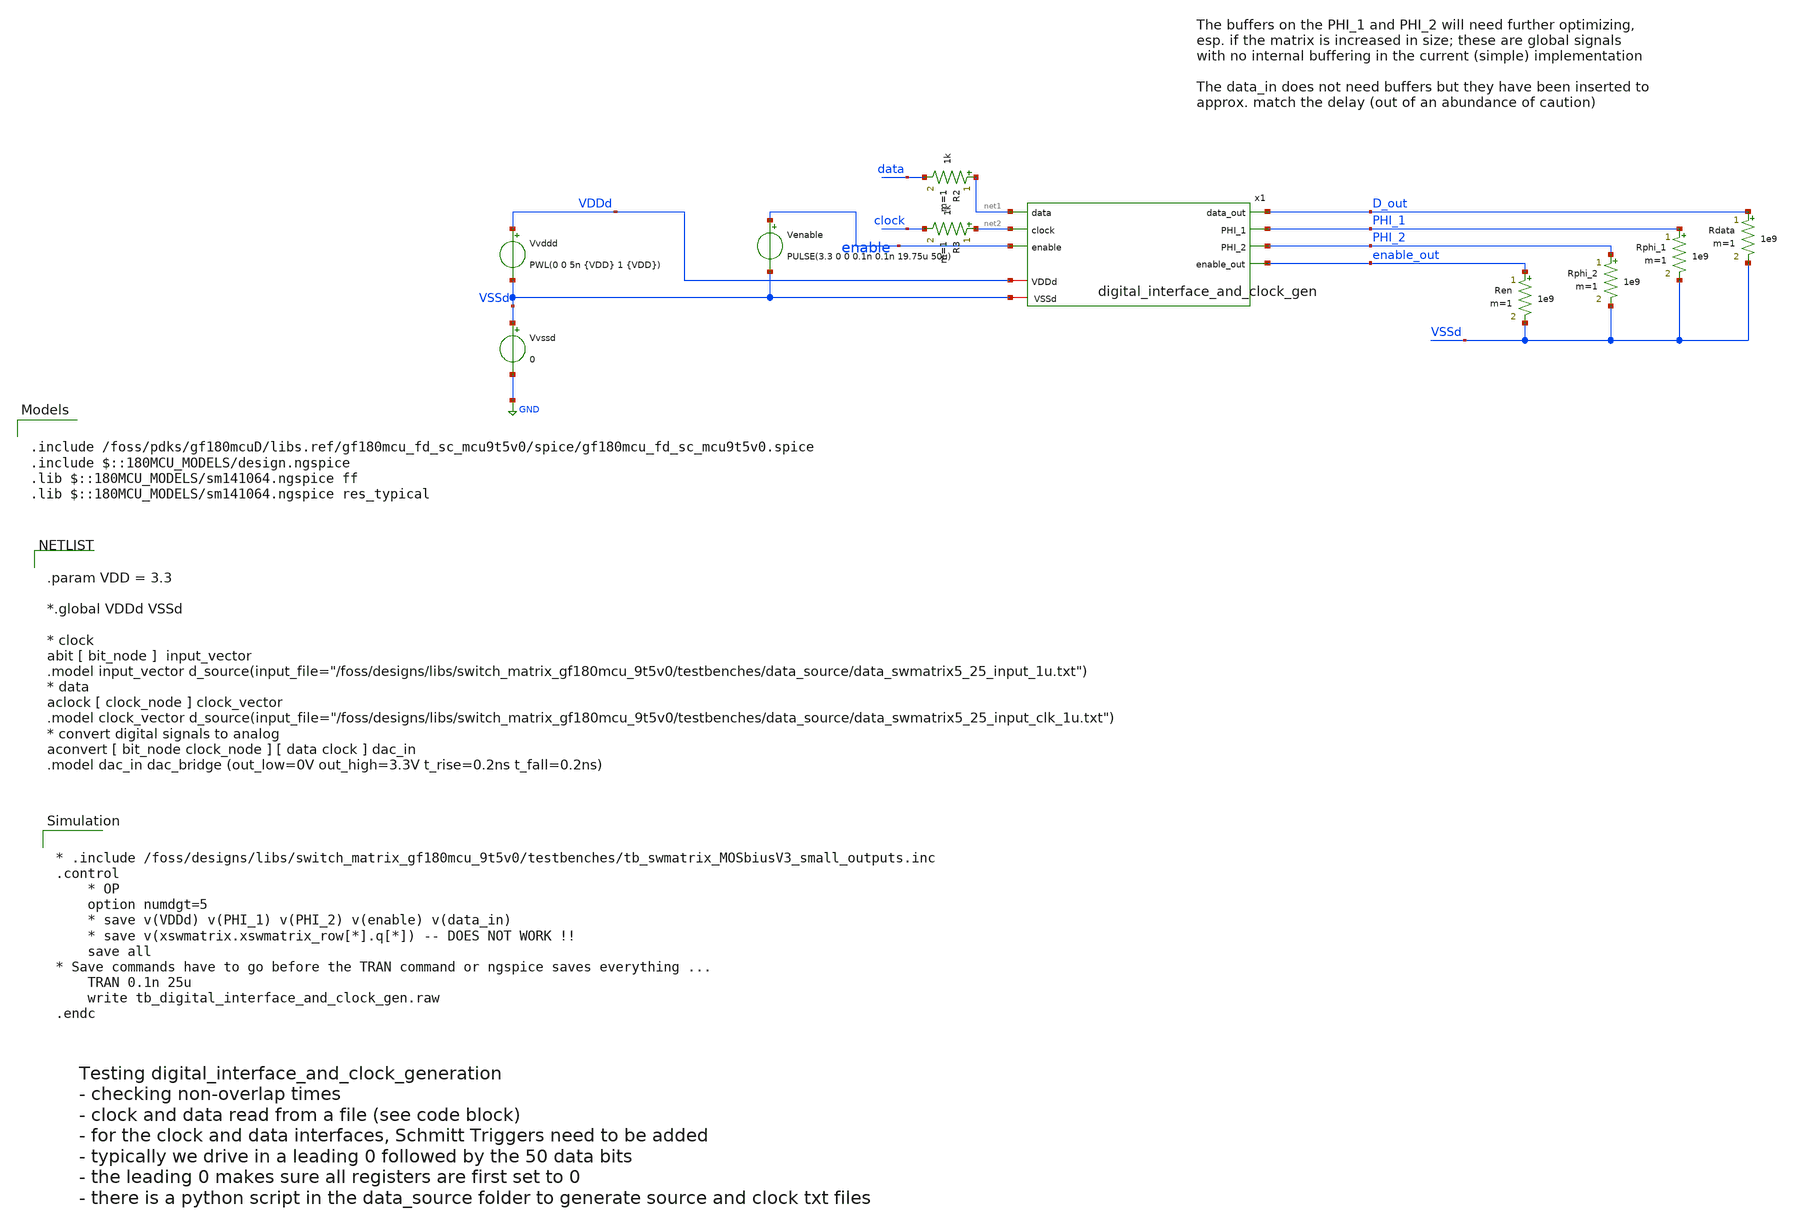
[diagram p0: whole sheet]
** sch_path: testbenches/tb_digital_interface_and_clock_gen.sch
**.subckt tb_digital_interface_and_clock_gen
Vvssd VSSd GND 0
Vvddd VDDd VSSd PWL(0 0 5n {VDD} 1 {VDD})
Venable enable VSSd PULSE(3.3 0 0 0.1n 0.1n 19.75u 50u)
R2 net1 data 1k m=1
R3 net2 clock 1k m=1
Ren enable_out VSSd 1e9 m=1
Rphi_2 PHI_2 VSSd 1e9 m=1
Rphi_1 PHI_1 VSSd 1e9 m=1
Rdata D_out VSSd 1e9 m=1
x1 net1 D_out net2 PHI_1 PHI_2 enable enable_out VDDd VSSd digital_interface_and_clock_gen
**** begin user architecture code


* .include
*+ /foss/designs/libs/switch_matrix_gf180mcu_9t5v0/testbenches/tb_swmatrix_MOSbiusV3_small_outputs.inc
.control
    * OP
    option numdgt=5
    * save v(VDDd) v(PHI_1) v(PHI_2) v(enable) v(data_in)
    * save v(xswmatrix.xswmatrix_row[*].q[*]) -- DOES NOT WORK !!
    save all
* Save commands have to go before the TRAN command or ngspice saves everything ...
    TRAN 0.1n 25u
    write tb_digital_interface_and_clock_gen.raw
.endc



.include /foss/pdks/gf180mcuD/libs.ref/gf180mcu_fd_sc_mcu9t5v0/spice/gf180mcu_fd_sc_mcu9t5v0.spice
.include $::180MCU_MODELS/design.ngspice
.lib $::180MCU_MODELS/sm141064.ngspice ff
.lib $::180MCU_MODELS/sm141064.ngspice res_typical



.param VDD = 3.3

*.global VDDd VSSd

* clock
abit [ bit_node ]  input_vector
.model input_vector
+ d_source(input_file="/foss/designs/libs/switch_matrix_gf180mcu_9t5v0/testbenches/data_source/data_swmatrix5_25_input_1u.txt")
* data
aclock [ clock_node ] clock_vector
.model clock_vector
+ d_source(input_file="/foss/designs/libs/switch_matrix_gf180mcu_9t5v0/testbenches/data_source/data_swmatrix5_25_input_clk_1u.txt")
* convert digital signals to analog
aconvert [ bit_node clock_node ] [ data clock ] dac_in
.model dac_in dac_bridge (out_low=0V out_high=3.3V t_rise=0.2ns t_fall=0.2ns)


**** end user architecture code
**.ends

* expanding   symbol:
*+  switch_matrix_gf180mcu_9t5v0/digital_interface_and_clock_gen/digital_interface_and_clock_gen.sym # of pins=9
** sym_path: digital_interface_and_clock_gen/digital_interface_and_clock_gen.sym
** sch_path: digital_interface_and_clock_gen/digital_interface_and_clock_gen.sch
.subckt digital_interface_and_clock_gen data data_out clock PHI_1 PHI_2 enable enable_out VDDd VSSd
*.ipin data
*.ipin clock
*.ipin enable
*.iopin VSSd
*.iopin VDDd
*.opin data_out
*.opin PHI_1
*.opin PHI_2
*.opin enable_out
xNO_ClkGen PHI_2_gen clock_gated PHI_1_gen VDDd VSSd NO_ClkGen
x6 PHI_2_gen VSSd VDDd VSSd VDDd net1 gf180mcu_fd_sc_mcu9t5v0__inv_4
x7 net1 VSSd VDDd VSSd VDDd PHI_2 gf180mcu_fd_sc_mcu9t5v0__inv_8
x9 PHI_1_gen VSSd VDDd VSSd VDDd net2 gf180mcu_fd_sc_mcu9t5v0__inv_4
x10 net2 VSSd VDDd VSSd VDDd PHI_1 gf180mcu_fd_sc_mcu9t5v0__inv_8
x12 data_gated VSSd VDDd VSSd VDDd net3 gf180mcu_fd_sc_mcu9t5v0__inv_4
x13 net3 VSSd VDDd VSSd VDDd net8 gf180mcu_fd_sc_mcu9t5v0__inv_8
x2 net7 VSSd VDDd VSSd VDDd net4 gf180mcu_fd_sc_mcu9t5v0__inv_4
x8 net4 VSSd VDDd VSSd VDDd enable_out gf180mcu_fd_sc_mcu9t5v0__inv_8
x11 net5 net4 VSSd VDDd VSSd VDDd net10 gf180mcu_fd_sc_mcu9t5v0__nand2_4
x4 net6 net4 VSSd VDDd VSSd VDDd net11 gf180mcu_fd_sc_mcu9t5v0__nand2_4
x1 net11 VSSd VDDd VSSd VDDd clock_gated gf180mcu_fd_sc_mcu9t5v0__inv_4
x3 net10 VSSd VDDd VSSd VDDd data_gated gf180mcu_fd_sc_mcu9t5v0__inv_4
x5 VDDd clock net6 VSSd Schmitt
x14 VDDd data net5 VSSd Schmitt
x15 VDDd enable net7 VSSd Schmitt
XR1 VSSd enable VSSd ppolyf_u_1k r_width=1e-6 r_length=20e-6 m=2
x16 net8 VSSd VDDd VSSd VDDd net9 gf180mcu_fd_sc_mcu9t5v0__inv_12
x17 net9 data_out VDDd VDDd VSSd VSSd gf180mcu_fd_sc_mcu9t5v0__inv_20
.ends


* expanding   symbol:  switch_matrix_gf180mcu_9t5v0/NO_ClkGen/NO_ClkGen.sym # of pins=5
** sym_path: switch_matrix_gf180mcu_9t5v0/NO_ClkGen/NO_ClkGen.sym
** sch_path: switch_matrix_gf180mcu_9t5v0/NO_ClkGen/NO_ClkGen.sch
.subckt NO_ClkGen PHI_2 CLK PHI_1 VDDd VSSd
*.ipin CLK
*.opin PHI_2
*.opin PHI_1
*.iopin VDDd
*.iopin VSSd
x1 CLKB OUT_bot_d VSSd VDDd VSSd VDDd OUT_top gf180mcu_fd_sc_mcu9t5v0__nand2_1
x2 OUT_top_d CLKbuf VSSd VDDd VSSd VDDd OUT_bot gf180mcu_fd_sc_mcu9t5v0__nand2_1
x3 OUT_top VSSd VDDd VSSd VDDd PHI_2 gf180mcu_fd_sc_mcu9t5v0__inv_1
x4 PHI_2 VSSd VDDd VSSd VDDd in_d_2 gf180mcu_fd_sc_mcu9t5v0__inv_1
x6 OUT_bot VSSd VDDd VSSd VDDd PHI_1 gf180mcu_fd_sc_mcu9t5v0__inv_1
x9 CLKB VSSd VDDd VSSd VDDd CLKbuf gf180mcu_fd_sc_mcu9t5v0__inv_1
x10 CLK VSSd VDDd VSSd VDDd CLKB gf180mcu_fd_sc_mcu9t5v0__inv_1
* noconn VDDd
* noconn VSSd
xinv1[1] in_d_2 VSSd VDDd VSSd VDDd out_2[1] gf180mcu_fd_sc_mcu9t5v0__inv_1
xinv1[2] out_2[1] VSSd VDDd VSSd VDDd out_2[2] gf180mcu_fd_sc_mcu9t5v0__inv_1
xinv1[3] out_2[2] VSSd VDDd VSSd VDDd out_2[3] gf180mcu_fd_sc_mcu9t5v0__inv_1
xinv1[4] out_2[3] VSSd VDDd VSSd VDDd out_2[4] gf180mcu_fd_sc_mcu9t5v0__inv_1
xinv1[5] out_2[4] VSSd VDDd VSSd VDDd out_2[5] gf180mcu_fd_sc_mcu9t5v0__inv_1
xinv1[6] out_2[5] VSSd VDDd VSSd VDDd out_2[6] gf180mcu_fd_sc_mcu9t5v0__inv_1
xinv1[7] out_2[6] VSSd VDDd VSSd VDDd out_2[7] gf180mcu_fd_sc_mcu9t5v0__inv_1
xinv1[8] out_2[7] VSSd VDDd VSSd VDDd out_2[8] gf180mcu_fd_sc_mcu9t5v0__inv_1
xinv1[9] out_2[8] VSSd VDDd VSSd VDDd out_2[9] gf180mcu_fd_sc_mcu9t5v0__inv_1
xinv1[10] out_2[9] VSSd VDDd VSSd VDDd out_2[10] gf180mcu_fd_sc_mcu9t5v0__inv_1
xinv1[11] out_2[10] VSSd VDDd VSSd VDDd out_2[11] gf180mcu_fd_sc_mcu9t5v0__inv_1
xinv1[12] out_2[11] VSSd VDDd VSSd VDDd out_2[12] gf180mcu_fd_sc_mcu9t5v0__inv_1
xinv1[13] out_2[12] VSSd VDDd VSSd VDDd out_2[13] gf180mcu_fd_sc_mcu9t5v0__inv_1
xinv1[14] out_2[13] VSSd VDDd VSSd VDDd out_2[14] gf180mcu_fd_sc_mcu9t5v0__inv_1
xinv1[15] out_2[14] VSSd VDDd VSSd VDDd out_2[15] gf180mcu_fd_sc_mcu9t5v0__inv_1
xinv1[16] out_2[15] VSSd VDDd VSSd VDDd out_2[16] gf180mcu_fd_sc_mcu9t5v0__inv_1
xinv1[17] out_2[16] VSSd VDDd VSSd VDDd out_2[17] gf180mcu_fd_sc_mcu9t5v0__inv_1
xinv1[18] out_2[17] VSSd VDDd VSSd VDDd out_2[18] gf180mcu_fd_sc_mcu9t5v0__inv_1
xinv1[19] out_2[18] VSSd VDDd VSSd VDDd out_2[19] gf180mcu_fd_sc_mcu9t5v0__inv_1
xinv1[20] out_2[19] VSSd VDDd VSSd VDDd OUT_top_d gf180mcu_fd_sc_mcu9t5v0__inv_1
x5 PHI_1 VSSd VDDd VSSd VDDd in_d_1 gf180mcu_fd_sc_mcu9t5v0__inv_1
xinv2[1] in_d_1 VSSd VDDd VSSd VDDd out_1[1] gf180mcu_fd_sc_mcu9t5v0__inv_1
xinv2[2] out_1[1] VSSd VDDd VSSd VDDd out_1[2] gf180mcu_fd_sc_mcu9t5v0__inv_1
xinv2[3] out_1[2] VSSd VDDd VSSd VDDd out_1[3] gf180mcu_fd_sc_mcu9t5v0__inv_1
xinv2[4] out_1[3] VSSd VDDd VSSd VDDd out_1[4] gf180mcu_fd_sc_mcu9t5v0__inv_1
xinv2[5] out_1[4] VSSd VDDd VSSd VDDd out_1[5] gf180mcu_fd_sc_mcu9t5v0__inv_1
xinv2[6] out_1[5] VSSd VDDd VSSd VDDd out_1[6] gf180mcu_fd_sc_mcu9t5v0__inv_1
xinv2[7] out_1[6] VSSd VDDd VSSd VDDd out_1[7] gf180mcu_fd_sc_mcu9t5v0__inv_1
xinv2[8] out_1[7] VSSd VDDd VSSd VDDd out_1[8] gf180mcu_fd_sc_mcu9t5v0__inv_1
xinv2[9] out_1[8] VSSd VDDd VSSd VDDd out_1[9] gf180mcu_fd_sc_mcu9t5v0__inv_1
xinv2[10] out_1[9] VSSd VDDd VSSd VDDd out_1[10] gf180mcu_fd_sc_mcu9t5v0__inv_1
xinv2[11] out_1[10] VSSd VDDd VSSd VDDd out_1[11] gf180mcu_fd_sc_mcu9t5v0__inv_1
xinv2[12] out_1[11] VSSd VDDd VSSd VDDd out_1[12] gf180mcu_fd_sc_mcu9t5v0__inv_1
xinv2[13] out_1[12] VSSd VDDd VSSd VDDd out_1[13] gf180mcu_fd_sc_mcu9t5v0__inv_1
xinv2[14] out_1[13] VSSd VDDd VSSd VDDd out_1[14] gf180mcu_fd_sc_mcu9t5v0__inv_1
xinv2[15] out_1[14] VSSd VDDd VSSd VDDd out_1[15] gf180mcu_fd_sc_mcu9t5v0__inv_1
xinv2[16] out_1[15] VSSd VDDd VSSd VDDd out_1[16] gf180mcu_fd_sc_mcu9t5v0__inv_1
xinv2[17] out_1[16] VSSd VDDd VSSd VDDd out_1[17] gf180mcu_fd_sc_mcu9t5v0__inv_1
xinv2[18] out_1[17] VSSd VDDd VSSd VDDd out_1[18] gf180mcu_fd_sc_mcu9t5v0__inv_1
xinv2[19] out_1[18] VSSd VDDd VSSd VDDd out_1[19] gf180mcu_fd_sc_mcu9t5v0__inv_1
xinv2[20] out_1[19] VSSd VDDd VSSd VDDd OUT_bot_d gf180mcu_fd_sc_mcu9t5v0__inv_1
XMcapbot[1] VSSd out_1[1] VSSd VSSd nfet_03v3 L=1u W=25u nf=5 ad='int((nf+1)/2) * W/nf * 0.18u' as='int((nf+2)/2) * W/nf * 0.18u'
+ pd='2*int((nf+1)/2) * (W/nf + 0.18u)' ps='2*int((nf+2)/2) * (W/nf + 0.18u)' nrd='0.18u / W' nrs='0.18u / W'
+ sa=0 sb=0 sd=0 m=1
XMcapbot[2] VSSd out_1[2] VSSd VSSd nfet_03v3 L=1u W=25u nf=5 ad='int((nf+1)/2) * W/nf * 0.18u' as='int((nf+2)/2) * W/nf * 0.18u'
+ pd='2*int((nf+1)/2) * (W/nf + 0.18u)' ps='2*int((nf+2)/2) * (W/nf + 0.18u)' nrd='0.18u / W' nrs='0.18u / W'
+ sa=0 sb=0 sd=0 m=1
XMcapbot[3] VSSd out_1[3] VSSd VSSd nfet_03v3 L=1u W=25u nf=5 ad='int((nf+1)/2) * W/nf * 0.18u' as='int((nf+2)/2) * W/nf * 0.18u'
+ pd='2*int((nf+1)/2) * (W/nf + 0.18u)' ps='2*int((nf+2)/2) * (W/nf + 0.18u)' nrd='0.18u / W' nrs='0.18u / W'
+ sa=0 sb=0 sd=0 m=1
XMcapbot[4] VSSd out_1[4] VSSd VSSd nfet_03v3 L=1u W=25u nf=5 ad='int((nf+1)/2) * W/nf * 0.18u' as='int((nf+2)/2) * W/nf * 0.18u'
+ pd='2*int((nf+1)/2) * (W/nf + 0.18u)' ps='2*int((nf+2)/2) * (W/nf + 0.18u)' nrd='0.18u / W' nrs='0.18u / W'
+ sa=0 sb=0 sd=0 m=1
XMcapbot[5] VSSd out_1[5] VSSd VSSd nfet_03v3 L=1u W=25u nf=5 ad='int((nf+1)/2) * W/nf * 0.18u' as='int((nf+2)/2) * W/nf * 0.18u'
+ pd='2*int((nf+1)/2) * (W/nf + 0.18u)' ps='2*int((nf+2)/2) * (W/nf + 0.18u)' nrd='0.18u / W' nrs='0.18u / W'
+ sa=0 sb=0 sd=0 m=1
XMcapbot[6] VSSd out_1[6] VSSd VSSd nfet_03v3 L=1u W=25u nf=5 ad='int((nf+1)/2) * W/nf * 0.18u' as='int((nf+2)/2) * W/nf * 0.18u'
+ pd='2*int((nf+1)/2) * (W/nf + 0.18u)' ps='2*int((nf+2)/2) * (W/nf + 0.18u)' nrd='0.18u / W' nrs='0.18u / W'
+ sa=0 sb=0 sd=0 m=1
XMcapbot[7] VSSd out_1[7] VSSd VSSd nfet_03v3 L=1u W=25u nf=5 ad='int((nf+1)/2) * W/nf * 0.18u' as='int((nf+2)/2) * W/nf * 0.18u'
+ pd='2*int((nf+1)/2) * (W/nf + 0.18u)' ps='2*int((nf+2)/2) * (W/nf + 0.18u)' nrd='0.18u / W' nrs='0.18u / W'
+ sa=0 sb=0 sd=0 m=1
XMcapbot[8] VSSd out_1[8] VSSd VSSd nfet_03v3 L=1u W=25u nf=5 ad='int((nf+1)/2) * W/nf * 0.18u' as='int((nf+2)/2) * W/nf * 0.18u'
+ pd='2*int((nf+1)/2) * (W/nf + 0.18u)' ps='2*int((nf+2)/2) * (W/nf + 0.18u)' nrd='0.18u / W' nrs='0.18u / W'
+ sa=0 sb=0 sd=0 m=1
XMcapbot[9] VSSd out_1[9] VSSd VSSd nfet_03v3 L=1u W=25u nf=5 ad='int((nf+1)/2) * W/nf * 0.18u' as='int((nf+2)/2) * W/nf * 0.18u'
+ pd='2*int((nf+1)/2) * (W/nf + 0.18u)' ps='2*int((nf+2)/2) * (W/nf + 0.18u)' nrd='0.18u / W' nrs='0.18u / W'
+ sa=0 sb=0 sd=0 m=1
XMcapbot[10] VSSd out_1[10] VSSd VSSd nfet_03v3 L=1u W=25u nf=5 ad='int((nf+1)/2) * W/nf * 0.18u' as='int((nf+2)/2) * W/nf * 0.18u'
+ pd='2*int((nf+1)/2) * (W/nf + 0.18u)' ps='2*int((nf+2)/2) * (W/nf + 0.18u)' nrd='0.18u / W' nrs='0.18u / W'
+ sa=0 sb=0 sd=0 m=1
XMcapbot[11] VSSd out_1[11] VSSd VSSd nfet_03v3 L=1u W=25u nf=5 ad='int((nf+1)/2) * W/nf * 0.18u' as='int((nf+2)/2) * W/nf * 0.18u'
+ pd='2*int((nf+1)/2) * (W/nf + 0.18u)' ps='2*int((nf+2)/2) * (W/nf + 0.18u)' nrd='0.18u / W' nrs='0.18u / W'
+ sa=0 sb=0 sd=0 m=1
XMcapbot[12] VSSd out_1[12] VSSd VSSd nfet_03v3 L=1u W=25u nf=5 ad='int((nf+1)/2) * W/nf * 0.18u' as='int((nf+2)/2) * W/nf * 0.18u'
+ pd='2*int((nf+1)/2) * (W/nf + 0.18u)' ps='2*int((nf+2)/2) * (W/nf + 0.18u)' nrd='0.18u / W' nrs='0.18u / W'
+ sa=0 sb=0 sd=0 m=1
XMcapbot[13] VSSd out_1[13] VSSd VSSd nfet_03v3 L=1u W=25u nf=5 ad='int((nf+1)/2) * W/nf * 0.18u' as='int((nf+2)/2) * W/nf * 0.18u'
+ pd='2*int((nf+1)/2) * (W/nf + 0.18u)' ps='2*int((nf+2)/2) * (W/nf + 0.18u)' nrd='0.18u / W' nrs='0.18u / W'
+ sa=0 sb=0 sd=0 m=1
XMcapbot[14] VSSd out_1[14] VSSd VSSd nfet_03v3 L=1u W=25u nf=5 ad='int((nf+1)/2) * W/nf * 0.18u' as='int((nf+2)/2) * W/nf * 0.18u'
+ pd='2*int((nf+1)/2) * (W/nf + 0.18u)' ps='2*int((nf+2)/2) * (W/nf + 0.18u)' nrd='0.18u / W' nrs='0.18u / W'
+ sa=0 sb=0 sd=0 m=1
XMcapbot[15] VSSd out_1[15] VSSd VSSd nfet_03v3 L=1u W=25u nf=5 ad='int((nf+1)/2) * W/nf * 0.18u' as='int((nf+2)/2) * W/nf * 0.18u'
+ pd='2*int((nf+1)/2) * (W/nf + 0.18u)' ps='2*int((nf+2)/2) * (W/nf + 0.18u)' nrd='0.18u / W' nrs='0.18u / W'
+ sa=0 sb=0 sd=0 m=1
XMcapbot[16] VSSd out_1[16] VSSd VSSd nfet_03v3 L=1u W=25u nf=5 ad='int((nf+1)/2) * W/nf * 0.18u' as='int((nf+2)/2) * W/nf * 0.18u'
+ pd='2*int((nf+1)/2) * (W/nf + 0.18u)' ps='2*int((nf+2)/2) * (W/nf + 0.18u)' nrd='0.18u / W' nrs='0.18u / W'
+ sa=0 sb=0 sd=0 m=1
XMcapbot[17] VSSd out_1[17] VSSd VSSd nfet_03v3 L=1u W=25u nf=5 ad='int((nf+1)/2) * W/nf * 0.18u' as='int((nf+2)/2) * W/nf * 0.18u'
+ pd='2*int((nf+1)/2) * (W/nf + 0.18u)' ps='2*int((nf+2)/2) * (W/nf + 0.18u)' nrd='0.18u / W' nrs='0.18u / W'
+ sa=0 sb=0 sd=0 m=1
XMcapbot[18] VSSd out_1[18] VSSd VSSd nfet_03v3 L=1u W=25u nf=5 ad='int((nf+1)/2) * W/nf * 0.18u' as='int((nf+2)/2) * W/nf * 0.18u'
+ pd='2*int((nf+1)/2) * (W/nf + 0.18u)' ps='2*int((nf+2)/2) * (W/nf + 0.18u)' nrd='0.18u / W' nrs='0.18u / W'
+ sa=0 sb=0 sd=0 m=1
XMcapbot[19] VSSd out_1[19] VSSd VSSd nfet_03v3 L=1u W=25u nf=5 ad='int((nf+1)/2) * W/nf * 0.18u' as='int((nf+2)/2) * W/nf * 0.18u'
+ pd='2*int((nf+1)/2) * (W/nf + 0.18u)' ps='2*int((nf+2)/2) * (W/nf + 0.18u)' nrd='0.18u / W' nrs='0.18u / W'
+ sa=0 sb=0 sd=0 m=1
XMcapbot[20] VSSd OUT_bot_d VSSd VSSd nfet_03v3 L=1u W=25u nf=5 ad='int((nf+1)/2) * W/nf * 0.18u' as='int((nf+2)/2) * W/nf * 0.18u'
+ pd='2*int((nf+1)/2) * (W/nf + 0.18u)' ps='2*int((nf+2)/2) * (W/nf + 0.18u)' nrd='0.18u / W' nrs='0.18u / W'
+ sa=0 sb=0 sd=0 m=1
XMcaptop[1] VSSd out_2[1] VSSd VSSd nfet_03v3 L=1u W=25u nf=5 ad='int((nf+1)/2) * W/nf * 0.18u' as='int((nf+2)/2) * W/nf * 0.18u'
+ pd='2*int((nf+1)/2) * (W/nf + 0.18u)' ps='2*int((nf+2)/2) * (W/nf + 0.18u)' nrd='0.18u / W' nrs='0.18u / W'
+ sa=0 sb=0 sd=0 m=1
XMcaptop[2] VSSd out_2[2] VSSd VSSd nfet_03v3 L=1u W=25u nf=5 ad='int((nf+1)/2) * W/nf * 0.18u' as='int((nf+2)/2) * W/nf * 0.18u'
+ pd='2*int((nf+1)/2) * (W/nf + 0.18u)' ps='2*int((nf+2)/2) * (W/nf + 0.18u)' nrd='0.18u / W' nrs='0.18u / W'
+ sa=0 sb=0 sd=0 m=1
XMcaptop[3] VSSd out_2[3] VSSd VSSd nfet_03v3 L=1u W=25u nf=5 ad='int((nf+1)/2) * W/nf * 0.18u' as='int((nf+2)/2) * W/nf * 0.18u'
+ pd='2*int((nf+1)/2) * (W/nf + 0.18u)' ps='2*int((nf+2)/2) * (W/nf + 0.18u)' nrd='0.18u / W' nrs='0.18u / W'
+ sa=0 sb=0 sd=0 m=1
XMcaptop[4] VSSd out_2[4] VSSd VSSd nfet_03v3 L=1u W=25u nf=5 ad='int((nf+1)/2) * W/nf * 0.18u' as='int((nf+2)/2) * W/nf * 0.18u'
+ pd='2*int((nf+1)/2) * (W/nf + 0.18u)' ps='2*int((nf+2)/2) * (W/nf + 0.18u)' nrd='0.18u / W' nrs='0.18u / W'
+ sa=0 sb=0 sd=0 m=1
XMcaptop[5] VSSd out_2[5] VSSd VSSd nfet_03v3 L=1u W=25u nf=5 ad='int((nf+1)/2) * W/nf * 0.18u' as='int((nf+2)/2) * W/nf * 0.18u'
+ pd='2*int((nf+1)/2) * (W/nf + 0.18u)' ps='2*int((nf+2)/2) * (W/nf + 0.18u)' nrd='0.18u / W' nrs='0.18u / W'
+ sa=0 sb=0 sd=0 m=1
XMcaptop[6] VSSd out_2[6] VSSd VSSd nfet_03v3 L=1u W=25u nf=5 ad='int((nf+1)/2) * W/nf * 0.18u' as='int((nf+2)/2) * W/nf * 0.18u'
+ pd='2*int((nf+1)/2) * (W/nf + 0.18u)' ps='2*int((nf+2)/2) * (W/nf + 0.18u)' nrd='0.18u / W' nrs='0.18u / W'
+ sa=0 sb=0 sd=0 m=1
XMcaptop[7] VSSd out_2[7] VSSd VSSd nfet_03v3 L=1u W=25u nf=5 ad='int((nf+1)/2) * W/nf * 0.18u' as='int((nf+2)/2) * W/nf * 0.18u'
+ pd='2*int((nf+1)/2) * (W/nf + 0.18u)' ps='2*int((nf+2)/2) * (W/nf + 0.18u)' nrd='0.18u / W' nrs='0.18u / W'
+ sa=0 sb=0 sd=0 m=1
XMcaptop[8] VSSd out_2[8] VSSd VSSd nfet_03v3 L=1u W=25u nf=5 ad='int((nf+1)/2) * W/nf * 0.18u' as='int((nf+2)/2) * W/nf * 0.18u'
+ pd='2*int((nf+1)/2) * (W/nf + 0.18u)' ps='2*int((nf+2)/2) * (W/nf + 0.18u)' nrd='0.18u / W' nrs='0.18u / W'
+ sa=0 sb=0 sd=0 m=1
XMcaptop[9] VSSd out_2[9] VSSd VSSd nfet_03v3 L=1u W=25u nf=5 ad='int((nf+1)/2) * W/nf * 0.18u' as='int((nf+2)/2) * W/nf * 0.18u'
+ pd='2*int((nf+1)/2) * (W/nf + 0.18u)' ps='2*int((nf+2)/2) * (W/nf + 0.18u)' nrd='0.18u / W' nrs='0.18u / W'
+ sa=0 sb=0 sd=0 m=1
XMcaptop[10] VSSd out_2[10] VSSd VSSd nfet_03v3 L=1u W=25u nf=5 ad='int((nf+1)/2) * W/nf * 0.18u' as='int((nf+2)/2) * W/nf * 0.18u'
+ pd='2*int((nf+1)/2) * (W/nf + 0.18u)' ps='2*int((nf+2)/2) * (W/nf + 0.18u)' nrd='0.18u / W' nrs='0.18u / W'
+ sa=0 sb=0 sd=0 m=1
XMcaptop[11] VSSd out_2[11] VSSd VSSd nfet_03v3 L=1u W=25u nf=5 ad='int((nf+1)/2) * W/nf * 0.18u' as='int((nf+2)/2) * W/nf * 0.18u'
+ pd='2*int((nf+1)/2) * (W/nf + 0.18u)' ps='2*int((nf+2)/2) * (W/nf + 0.18u)' nrd='0.18u / W' nrs='0.18u / W'
+ sa=0 sb=0 sd=0 m=1
XMcaptop[12] VSSd out_2[12] VSSd VSSd nfet_03v3 L=1u W=25u nf=5 ad='int((nf+1)/2) * W/nf * 0.18u' as='int((nf+2)/2) * W/nf * 0.18u'
+ pd='2*int((nf+1)/2) * (W/nf + 0.18u)' ps='2*int((nf+2)/2) * (W/nf + 0.18u)' nrd='0.18u / W' nrs='0.18u / W'
+ sa=0 sb=0 sd=0 m=1
XMcaptop[13] VSSd out_2[13] VSSd VSSd nfet_03v3 L=1u W=25u nf=5 ad='int((nf+1)/2) * W/nf * 0.18u' as='int((nf+2)/2) * W/nf * 0.18u'
+ pd='2*int((nf+1)/2) * (W/nf + 0.18u)' ps='2*int((nf+2)/2) * (W/nf + 0.18u)' nrd='0.18u / W' nrs='0.18u / W'
+ sa=0 sb=0 sd=0 m=1
XMcaptop[14] VSSd out_2[14] VSSd VSSd nfet_03v3 L=1u W=25u nf=5 ad='int((nf+1)/2) * W/nf * 0.18u' as='int((nf+2)/2) * W/nf * 0.18u'
+ pd='2*int((nf+1)/2) * (W/nf + 0.18u)' ps='2*int((nf+2)/2) * (W/nf + 0.18u)' nrd='0.18u / W' nrs='0.18u / W'
+ sa=0 sb=0 sd=0 m=1
XMcaptop[15] VSSd out_2[15] VSSd VSSd nfet_03v3 L=1u W=25u nf=5 ad='int((nf+1)/2) * W/nf * 0.18u' as='int((nf+2)/2) * W/nf * 0.18u'
+ pd='2*int((nf+1)/2) * (W/nf + 0.18u)' ps='2*int((nf+2)/2) * (W/nf + 0.18u)' nrd='0.18u / W' nrs='0.18u / W'
+ sa=0 sb=0 sd=0 m=1
XMcaptop[16] VSSd out_2[16] VSSd VSSd nfet_03v3 L=1u W=25u nf=5 ad='int((nf+1)/2) * W/nf * 0.18u' as='int((nf+2)/2) * W/nf * 0.18u'
+ pd='2*int((nf+1)/2) * (W/nf + 0.18u)' ps='2*int((nf+2)/2) * (W/nf + 0.18u)' nrd='0.18u / W' nrs='0.18u / W'
+ sa=0 sb=0 sd=0 m=1
XMcaptop[17] VSSd out_2[17] VSSd VSSd nfet_03v3 L=1u W=25u nf=5 ad='int((nf+1)/2) * W/nf * 0.18u' as='int((nf+2)/2) * W/nf * 0.18u'
+ pd='2*int((nf+1)/2) * (W/nf + 0.18u)' ps='2*int((nf+2)/2) * (W/nf + 0.18u)' nrd='0.18u / W' nrs='0.18u / W'
+ sa=0 sb=0 sd=0 m=1
XMcaptop[18] VSSd out_2[18] VSSd VSSd nfet_03v3 L=1u W=25u nf=5 ad='int((nf+1)/2) * W/nf * 0.18u' as='int((nf+2)/2) * W/nf * 0.18u'
+ pd='2*int((nf+1)/2) * (W/nf + 0.18u)' ps='2*int((nf+2)/2) * (W/nf + 0.18u)' nrd='0.18u / W' nrs='0.18u / W'
+ sa=0 sb=0 sd=0 m=1
XMcaptop[19] VSSd out_2[19] VSSd VSSd nfet_03v3 L=1u W=25u nf=5 ad='int((nf+1)/2) * W/nf * 0.18u' as='int((nf+2)/2) * W/nf * 0.18u'
+ pd='2*int((nf+1)/2) * (W/nf + 0.18u)' ps='2*int((nf+2)/2) * (W/nf + 0.18u)' nrd='0.18u / W' nrs='0.18u / W'
+ sa=0 sb=0 sd=0 m=1
XMcaptop[20] VSSd OUT_top_d VSSd VSSd nfet_03v3 L=1u W=25u nf=5 ad='int((nf+1)/2) * W/nf * 0.18u' as='int((nf+2)/2) * W/nf * 0.18u'
+ pd='2*int((nf+1)/2) * (W/nf + 0.18u)' ps='2*int((nf+2)/2) * (W/nf + 0.18u)' nrd='0.18u / W' nrs='0.18u / W'
+ sa=0 sb=0 sd=0 m=1
XMcapbotp[1] VDDd out_1[1] VDDd VDDd pfet_03v3 L=1u W=25u nf=5 ad='int((nf+1)/2) * W/nf * 0.18u' as='int((nf+2)/2) * W/nf * 0.18u'
+ pd='2*int((nf+1)/2) * (W/nf + 0.18u)' ps='2*int((nf+2)/2) * (W/nf + 0.18u)' nrd='0.18u / W' nrs='0.18u / W'
+ sa=0 sb=0 sd=0 m=1
XMcapbotp[2] VDDd out_1[2] VDDd VDDd pfet_03v3 L=1u W=25u nf=5 ad='int((nf+1)/2) * W/nf * 0.18u' as='int((nf+2)/2) * W/nf * 0.18u'
+ pd='2*int((nf+1)/2) * (W/nf + 0.18u)' ps='2*int((nf+2)/2) * (W/nf + 0.18u)' nrd='0.18u / W' nrs='0.18u / W'
+ sa=0 sb=0 sd=0 m=1
XMcapbotp[3] VDDd out_1[3] VDDd VDDd pfet_03v3 L=1u W=25u nf=5 ad='int((nf+1)/2) * W/nf * 0.18u' as='int((nf+2)/2) * W/nf * 0.18u'
+ pd='2*int((nf+1)/2) * (W/nf + 0.18u)' ps='2*int((nf+2)/2) * (W/nf + 0.18u)' nrd='0.18u / W' nrs='0.18u / W'
+ sa=0 sb=0 sd=0 m=1
XMcapbotp[4] VDDd out_1[4] VDDd VDDd pfet_03v3 L=1u W=25u nf=5 ad='int((nf+1)/2) * W/nf * 0.18u' as='int((nf+2)/2) * W/nf * 0.18u'
+ pd='2*int((nf+1)/2) * (W/nf + 0.18u)' ps='2*int((nf+2)/2) * (W/nf + 0.18u)' nrd='0.18u / W' nrs='0.18u / W'
+ sa=0 sb=0 sd=0 m=1
XMcapbotp[5] VDDd out_1[5] VDDd VDDd pfet_03v3 L=1u W=25u nf=5 ad='int((nf+1)/2) * W/nf * 0.18u' as='int((nf+2)/2) * W/nf * 0.18u'
+ pd='2*int((nf+1)/2) * (W/nf + 0.18u)' ps='2*int((nf+2)/2) * (W/nf + 0.18u)' nrd='0.18u / W' nrs='0.18u / W'
+ sa=0 sb=0 sd=0 m=1
XMcapbotp[6] VDDd out_1[6] VDDd VDDd pfet_03v3 L=1u W=25u nf=5 ad='int((nf+1)/2) * W/nf * 0.18u' as='int((nf+2)/2) * W/nf * 0.18u'
+ pd='2*int((nf+1)/2) * (W/nf + 0.18u)' ps='2*int((nf+2)/2) * (W/nf + 0.18u)' nrd='0.18u / W' nrs='0.18u / W'
+ sa=0 sb=0 sd=0 m=1
XMcapbotp[7] VDDd out_1[7] VDDd VDDd pfet_03v3 L=1u W=25u nf=5 ad='int((nf+1)/2) * W/nf * 0.18u' as='int((nf+2)/2) * W/nf * 0.18u'
+ pd='2*int((nf+1)/2) * (W/nf + 0.18u)' ps='2*int((nf+2)/2) * (W/nf + 0.18u)' nrd='0.18u / W' nrs='0.18u / W'
+ sa=0 sb=0 sd=0 m=1
XMcapbotp[8] VDDd out_1[8] VDDd VDDd pfet_03v3 L=1u W=25u nf=5 ad='int((nf+1)/2) * W/nf * 0.18u' as='int((nf+2)/2) * W/nf * 0.18u'
+ pd='2*int((nf+1)/2) * (W/nf + 0.18u)' ps='2*int((nf+2)/2) * (W/nf + 0.18u)' nrd='0.18u / W' nrs='0.18u / W'
+ sa=0 sb=0 sd=0 m=1
XMcapbotp[9] VDDd out_1[9] VDDd VDDd pfet_03v3 L=1u W=25u nf=5 ad='int((nf+1)/2) * W/nf * 0.18u' as='int((nf+2)/2) * W/nf * 0.18u'
+ pd='2*int((nf+1)/2) * (W/nf + 0.18u)' ps='2*int((nf+2)/2) * (W/nf + 0.18u)' nrd='0.18u / W' nrs='0.18u / W'
+ sa=0 sb=0 sd=0 m=1
XMcapbotp[10] VDDd out_1[10] VDDd VDDd pfet_03v3 L=1u W=25u nf=5 ad='int((nf+1)/2) * W/nf * 0.18u' as='int((nf+2)/2) * W/nf * 0.18u'
+ pd='2*int((nf+1)/2) * (W/nf + 0.18u)' ps='2*int((nf+2)/2) * (W/nf + 0.18u)' nrd='0.18u / W' nrs='0.18u / W'
+ sa=0 sb=0 sd=0 m=1
XMcapbotp[11] VDDd out_1[11] VDDd VDDd pfet_03v3 L=1u W=25u nf=5 ad='int((nf+1)/2) * W/nf * 0.18u' as='int((nf+2)/2) * W/nf * 0.18u'
+ pd='2*int((nf+1)/2) * (W/nf + 0.18u)' ps='2*int((nf+2)/2) * (W/nf + 0.18u)' nrd='0.18u / W' nrs='0.18u / W'
+ sa=0 sb=0 sd=0 m=1
XMcapbotp[12] VDDd out_1[12] VDDd VDDd pfet_03v3 L=1u W=25u nf=5 ad='int((nf+1)/2) * W/nf * 0.18u' as='int((nf+2)/2) * W/nf * 0.18u'
+ pd='2*int((nf+1)/2) * (W/nf + 0.18u)' ps='2*int((nf+2)/2) * (W/nf + 0.18u)' nrd='0.18u / W' nrs='0.18u / W'
+ sa=0 sb=0 sd=0 m=1
XMcapbotp[13] VDDd out_1[13] VDDd VDDd pfet_03v3 L=1u W=25u nf=5 ad='int((nf+1)/2) * W/nf * 0.18u' as='int((nf+2)/2) * W/nf * 0.18u'
+ pd='2*int((nf+1)/2) * (W/nf + 0.18u)' ps='2*int((nf+2)/2) * (W/nf + 0.18u)' nrd='0.18u / W' nrs='0.18u / W'
+ sa=0 sb=0 sd=0 m=1
XMcapbotp[14] VDDd out_1[14] VDDd VDDd pfet_03v3 L=1u W=25u nf=5 ad='int((nf+1)/2) * W/nf * 0.18u' as='int((nf+2)/2) * W/nf * 0.18u'
+ pd='2*int((nf+1)/2) * (W/nf + 0.18u)' ps='2*int((nf+2)/2) * (W/nf + 0.18u)' nrd='0.18u / W' nrs='0.18u / W'
+ sa=0 sb=0 sd=0 m=1
XMcapbotp[15] VDDd out_1[15] VDDd VDDd pfet_03v3 L=1u W=25u nf=5 ad='int((nf+1)/2) * W/nf * 0.18u' as='int((nf+2)/2) * W/nf * 0.18u'
+ pd='2*int((nf+1)/2) * (W/nf + 0.18u)' ps='2*int((nf+2)/2) * (W/nf + 0.18u)' nrd='0.18u / W' nrs='0.18u / W'
+ sa=0 sb=0 sd=0 m=1
XMcapbotp[16] VDDd out_1[16] VDDd VDDd pfet_03v3 L=1u W=25u nf=5 ad='int((nf+1)/2) * W/nf * 0.18u' as='int((nf+2)/2) * W/nf * 0.18u'
+ pd='2*int((nf+1)/2) * (W/nf + 0.18u)' ps='2*int((nf+2)/2) * (W/nf + 0.18u)' nrd='0.18u / W' nrs='0.18u / W'
+ sa=0 sb=0 sd=0 m=1
XMcapbotp[17] VDDd out_1[17] VDDd VDDd pfet_03v3 L=1u W=25u nf=5 ad='int((nf+1)/2) * W/nf * 0.18u' as='int((nf+2)/2) * W/nf * 0.18u'
+ pd='2*int((nf+1)/2) * (W/nf + 0.18u)' ps='2*int((nf+2)/2) * (W/nf + 0.18u)' nrd='0.18u / W' nrs='0.18u / W'
+ sa=0 sb=0 sd=0 m=1
XMcapbotp[18] VDDd out_1[18] VDDd VDDd pfet_03v3 L=1u W=25u nf=5 ad='int((nf+1)/2) * W/nf * 0.18u' as='int((nf+2)/2) * W/nf * 0.18u'
+ pd='2*int((nf+1)/2) * (W/nf + 0.18u)' ps='2*int((nf+2)/2) * (W/nf + 0.18u)' nrd='0.18u / W' nrs='0.18u / W'
+ sa=0 sb=0 sd=0 m=1
XMcapbotp[19] VDDd out_1[19] VDDd VDDd pfet_03v3 L=1u W=25u nf=5 ad='int((nf+1)/2) * W/nf * 0.18u' as='int((nf+2)/2) * W/nf * 0.18u'
+ pd='2*int((nf+1)/2) * (W/nf + 0.18u)' ps='2*int((nf+2)/2) * (W/nf + 0.18u)' nrd='0.18u / W' nrs='0.18u / W'
+ sa=0 sb=0 sd=0 m=1
XMcapbotp[20] VDDd OUT_bot_d VDDd VDDd pfet_03v3 L=1u W=25u nf=5 ad='int((nf+1)/2) * W/nf * 0.18u' as='int((nf+2)/2) * W/nf * 0.18u'
+ pd='2*int((nf+1)/2) * (W/nf + 0.18u)' ps='2*int((nf+2)/2) * (W/nf + 0.18u)' nrd='0.18u / W' nrs='0.18u / W'
+ sa=0 sb=0 sd=0 m=1
XMcaptopp[1] VDDd out_2[1] VDDd VDDd pfet_03v3 L=1u W=25u nf=5 ad='int((nf+1)/2) * W/nf * 0.18u' as='int((nf+2)/2) * W/nf * 0.18u'
+ pd='2*int((nf+1)/2) * (W/nf + 0.18u)' ps='2*int((nf+2)/2) * (W/nf + 0.18u)' nrd='0.18u / W' nrs='0.18u / W'
+ sa=0 sb=0 sd=0 m=1
XMcaptopp[2] VDDd out_2[2] VDDd VDDd pfet_03v3 L=1u W=25u nf=5 ad='int((nf+1)/2) * W/nf * 0.18u' as='int((nf+2)/2) * W/nf * 0.18u'
+ pd='2*int((nf+1)/2) * (W/nf + 0.18u)' ps='2*int((nf+2)/2) * (W/nf + 0.18u)' nrd='0.18u / W' nrs='0.18u / W'
+ sa=0 sb=0 sd=0 m=1
XMcaptopp[3] VDDd out_2[3] VDDd VDDd pfet_03v3 L=1u W=25u nf=5 ad='int((nf+1)/2) * W/nf * 0.18u' as='int((nf+2)/2) * W/nf * 0.18u'
+ pd='2*int((nf+1)/2) * (W/nf + 0.18u)' ps='2*int((nf+2)/2) * (W/nf + 0.18u)' nrd='0.18u / W' nrs='0.18u / W'
+ sa=0 sb=0 sd=0 m=1
XMcaptopp[4] VDDd out_2[4] VDDd VDDd pfet_03v3 L=1u W=25u nf=5 ad='int((nf+1)/2) * W/nf * 0.18u' as='int((nf+2)/2) * W/nf * 0.18u'
+ pd='2*int((nf+1)/2) * (W/nf + 0.18u)' ps='2*int((nf+2)/2) * (W/nf + 0.18u)' nrd='0.18u / W' nrs='0.18u / W'
+ sa=0 sb=0 sd=0 m=1
XMcaptopp[5] VDDd out_2[5] VDDd VDDd pfet_03v3 L=1u W=25u nf=5 ad='int((nf+1)/2) * W/nf * 0.18u' as='int((nf+2)/2) * W/nf * 0.18u'
+ pd='2*int((nf+1)/2) * (W/nf + 0.18u)' ps='2*int((nf+2)/2) * (W/nf + 0.18u)' nrd='0.18u / W' nrs='0.18u / W'
+ sa=0 sb=0 sd=0 m=1
XMcaptopp[6] VDDd out_2[6] VDDd VDDd pfet_03v3 L=1u W=25u nf=5 ad='int((nf+1)/2) * W/nf * 0.18u' as='int((nf+2)/2) * W/nf * 0.18u'
+ pd='2*int((nf+1)/2) * (W/nf + 0.18u)' ps='2*int((nf+2)/2) * (W/nf + 0.18u)' nrd='0.18u / W' nrs='0.18u / W'
+ sa=0 sb=0 sd=0 m=1
XMcaptopp[7] VDDd out_2[7] VDDd VDDd pfet_03v3 L=1u W=25u nf=5 ad='int((nf+1)/2) * W/nf * 0.18u' as='int((nf+2)/2) * W/nf * 0.18u'
+ pd='2*int((nf+1)/2) * (W/nf + 0.18u)' ps='2*int((nf+2)/2) * (W/nf + 0.18u)' nrd='0.18u / W' nrs='0.18u / W'
+ sa=0 sb=0 sd=0 m=1
XMcaptopp[8] VDDd out_2[8] VDDd VDDd pfet_03v3 L=1u W=25u nf=5 ad='int((nf+1)/2) * W/nf * 0.18u' as='int((nf+2)/2) * W/nf * 0.18u'
+ pd='2*int((nf+1)/2) * (W/nf + 0.18u)' ps='2*int((nf+2)/2) * (W/nf + 0.18u)' nrd='0.18u / W' nrs='0.18u / W'
+ sa=0 sb=0 sd=0 m=1
XMcaptopp[9] VDDd out_2[9] VDDd VDDd pfet_03v3 L=1u W=25u nf=5 ad='int((nf+1)/2) * W/nf * 0.18u' as='int((nf+2)/2) * W/nf * 0.18u'
+ pd='2*int((nf+1)/2) * (W/nf + 0.18u)' ps='2*int((nf+2)/2) * (W/nf + 0.18u)' nrd='0.18u / W' nrs='0.18u / W'
+ sa=0 sb=0 sd=0 m=1
XMcaptopp[10] VDDd out_2[10] VDDd VDDd pfet_03v3 L=1u W=25u nf=5 ad='int((nf+1)/2) * W/nf * 0.18u' as='int((nf+2)/2) * W/nf * 0.18u'
+ pd='2*int((nf+1)/2) * (W/nf + 0.18u)' ps='2*int((nf+2)/2) * (W/nf + 0.18u)' nrd='0.18u / W' nrs='0.18u / W'
+ sa=0 sb=0 sd=0 m=1
XMcaptopp[11] VDDd out_2[11] VDDd VDDd pfet_03v3 L=1u W=25u nf=5 ad='int((nf+1)/2) * W/nf * 0.18u' as='int((nf+2)/2) * W/nf * 0.18u'
+ pd='2*int((nf+1)/2) * (W/nf + 0.18u)' ps='2*int((nf+2)/2) * (W/nf + 0.18u)' nrd='0.18u / W' nrs='0.18u / W'
+ sa=0 sb=0 sd=0 m=1
XMcaptopp[12] VDDd out_2[12] VDDd VDDd pfet_03v3 L=1u W=25u nf=5 ad='int((nf+1)/2) * W/nf * 0.18u' as='int((nf+2)/2) * W/nf * 0.18u'
+ pd='2*int((nf+1)/2) * (W/nf + 0.18u)' ps='2*int((nf+2)/2) * (W/nf + 0.18u)' nrd='0.18u / W' nrs='0.18u / W'
+ sa=0 sb=0 sd=0 m=1
XMcaptopp[13] VDDd out_2[13] VDDd VDDd pfet_03v3 L=1u W=25u nf=5 ad='int((nf+1)/2) * W/nf * 0.18u' as='int((nf+2)/2) * W/nf * 0.18u'
+ pd='2*int((nf+1)/2) * (W/nf + 0.18u)' ps='2*int((nf+2)/2) * (W/nf + 0.18u)' nrd='0.18u / W' nrs='0.18u / W'
+ sa=0 sb=0 sd=0 m=1
XMcaptopp[14] VDDd out_2[14] VDDd VDDd pfet_03v3 L=1u W=25u nf=5 ad='int((nf+1)/2) * W/nf * 0.18u' as='int((nf+2)/2) * W/nf * 0.18u'
+ pd='2*int((nf+1)/2) * (W/nf + 0.18u)' ps='2*int((nf+2)/2) * (W/nf + 0.18u)' nrd='0.18u / W' nrs='0.18u / W'
+ sa=0 sb=0 sd=0 m=1
XMcaptopp[15] VDDd out_2[15] VDDd VDDd pfet_03v3 L=1u W=25u nf=5 ad='int((nf+1)/2) * W/nf * 0.18u' as='int((nf+2)/2) * W/nf * 0.18u'
+ pd='2*int((nf+1)/2) * (W/nf + 0.18u)' ps='2*int((nf+2)/2) * (W/nf + 0.18u)' nrd='0.18u / W' nrs='0.18u / W'
+ sa=0 sb=0 sd=0 m=1
XMcaptopp[16] VDDd out_2[16] VDDd VDDd pfet_03v3 L=1u W=25u nf=5 ad='int((nf+1)/2) * W/nf * 0.18u' as='int((nf+2)/2) * W/nf * 0.18u'
+ pd='2*int((nf+1)/2) * (W/nf + 0.18u)' ps='2*int((nf+2)/2) * (W/nf + 0.18u)' nrd='0.18u / W' nrs='0.18u / W'
+ sa=0 sb=0 sd=0 m=1
XMcaptopp[17] VDDd out_2[17] VDDd VDDd pfet_03v3 L=1u W=25u nf=5 ad='int((nf+1)/2) * W/nf * 0.18u' as='int((nf+2)/2) * W/nf * 0.18u'
+ pd='2*int((nf+1)/2) * (W/nf + 0.18u)' ps='2*int((nf+2)/2) * (W/nf + 0.18u)' nrd='0.18u / W' nrs='0.18u / W'
+ sa=0 sb=0 sd=0 m=1
XMcaptopp[18] VDDd out_2[18] VDDd VDDd pfet_03v3 L=1u W=25u nf=5 ad='int((nf+1)/2) * W/nf * 0.18u' as='int((nf+2)/2) * W/nf * 0.18u'
+ pd='2*int((nf+1)/2) * (W/nf + 0.18u)' ps='2*int((nf+2)/2) * (W/nf + 0.18u)' nrd='0.18u / W' nrs='0.18u / W'
+ sa=0 sb=0 sd=0 m=1
XMcaptopp[19] VDDd out_2[19] VDDd VDDd pfet_03v3 L=1u W=25u nf=5 ad='int((nf+1)/2) * W/nf * 0.18u' as='int((nf+2)/2) * W/nf * 0.18u'
+ pd='2*int((nf+1)/2) * (W/nf + 0.18u)' ps='2*int((nf+2)/2) * (W/nf + 0.18u)' nrd='0.18u / W' nrs='0.18u / W'
+ sa=0 sb=0 sd=0 m=1
XMcaptopp[20] VDDd OUT_top_d VDDd VDDd pfet_03v3 L=1u W=25u nf=5 ad='int((nf+1)/2) * W/nf * 0.18u' as='int((nf+2)/2) * W/nf * 0.18u'
+ pd='2*int((nf+1)/2) * (W/nf + 0.18u)' ps='2*int((nf+2)/2) * (W/nf + 0.18u)' nrd='0.18u / W' nrs='0.18u / W'
+ sa=0 sb=0 sd=0 m=1
.ends


* expanding   symbol:  switch_matrix_gf180mcu_9t5v0/Schmitt/Schmitt.sym # of pins=4
** sym_path: Schmitt/Schmitt.sym
** sch_path: Schmitt/Schmitt.sch
.subckt Schmitt VDD Vin Vo VSS
*.ipin VDD
*.ipin VSS
*.ipin Vin
*.opin Vo
XM9 schmitt Vin bot VSS nfet_06v0 L=0.70u W=2u nf=2 ad='int((nf+1)/2) * W/nf * 0.18u' as='int((nf+2)/2) * W/nf * 0.18u'
+ pd='2*int((nf+1)/2) * (W/nf + 0.18u)' ps='2*int((nf+2)/2) * (W/nf + 0.18u)' nrd='0.18u / W' nrs='0.18u / W'
+ sa=0 sb=0 sd=0 m=1
XM10 schmitt Vin top VDD pfet_06v0 L=0.55u W=6u nf=2 ad='int((nf+1)/2) * W/nf * 0.18u' as='int((nf+2)/2) * W/nf * 0.18u'
+ pd='2*int((nf+1)/2) * (W/nf + 0.18u)' ps='2*int((nf+2)/2) * (W/nf + 0.18u)' nrd='0.18u / W' nrs='0.18u / W'
+ sa=0 sb=0 sd=0 m=1
XM11 VDD schmitt bot VSS nfet_06v0 L=0.70u W=2u nf=2 ad='int((nf+1)/2) * W/nf * 0.18u' as='int((nf+2)/2) * W/nf * 0.18u'
+ pd='2*int((nf+1)/2) * (W/nf + 0.18u)' ps='2*int((nf+2)/2) * (W/nf + 0.18u)' nrd='0.18u / W' nrs='0.18u / W'
+ sa=0 sb=0 sd=0 m=1
XM12 top Vin VDD VDD pfet_06v0 L=0.55u W=6u nf=2 ad='int((nf+1)/2) * W/nf * 0.18u' as='int((nf+2)/2) * W/nf * 0.18u'
+ pd='2*int((nf+1)/2) * (W/nf + 0.18u)' ps='2*int((nf+2)/2) * (W/nf + 0.18u)' nrd='0.18u / W' nrs='0.18u / W'
+ sa=0 sb=0 sd=0 m=1
XM13 Vo schmitt VSS VSS nfet_06v0 L=0.70u W=2u nf=2 ad='int((nf+1)/2) * W/nf * 0.18u' as='int((nf+2)/2) * W/nf * 0.18u'
+ pd='2*int((nf+1)/2) * (W/nf + 0.18u)' ps='2*int((nf+2)/2) * (W/nf + 0.18u)' nrd='0.18u / W' nrs='0.18u / W'
+ sa=0 sb=0 sd=0 m=1
XM14 Vo schmitt VDD VDD pfet_06v0 L=0.55u W=6u nf=2 ad='int((nf+1)/2) * W/nf * 0.18u' as='int((nf+2)/2) * W/nf * 0.18u'
+ pd='2*int((nf+1)/2) * (W/nf + 0.18u)' ps='2*int((nf+2)/2) * (W/nf + 0.18u)' nrd='0.18u / W' nrs='0.18u / W'
+ sa=0 sb=0 sd=0 m=1
XM15 VSS schmitt top VDD pfet_06v0 L=0.55u W=6u nf=2 ad='int((nf+1)/2) * W/nf * 0.18u' as='int((nf+2)/2) * W/nf * 0.18u'
+ pd='2*int((nf+1)/2) * (W/nf + 0.18u)' ps='2*int((nf+2)/2) * (W/nf + 0.18u)' nrd='0.18u / W' nrs='0.18u / W'
+ sa=0 sb=0 sd=0 m=1
XM1 bot Vin VSS VSS nfet_06v0 L=0.70u W=2u nf=2 ad='int((nf+1)/2) * W/nf * 0.18u' as='int((nf+2)/2) * W/nf * 0.18u'
+ pd='2*int((nf+1)/2) * (W/nf + 0.18u)' ps='2*int((nf+2)/2) * (W/nf + 0.18u)' nrd='0.18u / W' nrs='0.18u / W'
+ sa=0 sb=0 sd=0 m=1
.ends

.GLOBAL GND
.end
